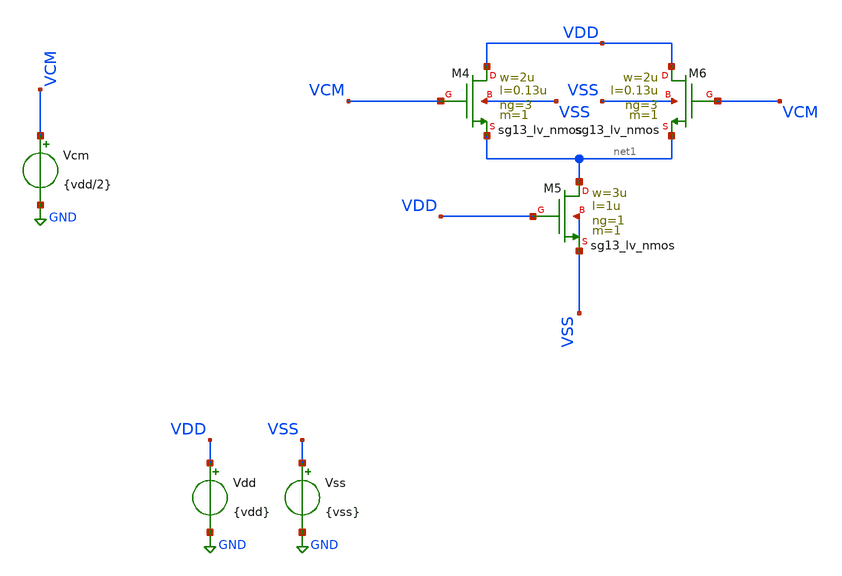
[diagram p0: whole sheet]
** sch_path: designs/comparator_noise/comparator_tb.sch
**.subckt comparator_tb
Vdd VDD GND {vdd}
Vss VSS GND {vss}
Vcm VCM GND {vdd/2}
XM4 VDD VCM net1 VSS sg13_lv_nmos w=2u l=0.13u ng=3 m=1 mm_ok=1
XM5 net1 VDD VSS VSS sg13_lv_nmos w=3u l=1u ng=1 m=1 mm_ok=1
XM6 VDD VCM net1 VSS sg13_lv_nmos w=2u l=0.13u ng=3 m=1 mm_ok=1
**** begin user architecture code

.lib $::SG13G2_MODELS/cornerMOSlv.lib mos_tt
.lib $::SG13G2_MODELS/cornerCAP.lib cap_typ
.include $::PDK_ROOT/ihp-sg13g2/libs.ref/sg13g2_stdcell/spice/sg13g2_stdcell.spice




.param vss=0
.param vdd=1.5

.control
	save all
	op

	print @n.xm4.nsg13_lv_nmos[gm]
	print @n.xm6.nsg13_lv_nmos[gm]

  * --- node P  ----------------------------------------------------
  let CP =  @n.xm4.nsg13_lv_nmos[cdb]      ; drain‐to‐bulk M4
           +@n.xm4.nsg13_lv_nmos[cgs]      ; gate–source overlap M4
           +@n.xm4.nsg13_lv_nmos[cgd]       ; gate–drain overlap  M4

  * --- node Q  ----------------------------------------------------
  let CQ =  @n.xm6.nsg13_lv_nmos[cdb]
           +@n.xm6.nsg13_lv_nmos[cgs]
           +@n.xm6.nsg13_lv_nmos[cgd]

  print CP
  print CQ
.endc



**** end user architecture code
**.ends
.GLOBAL GND
.end
